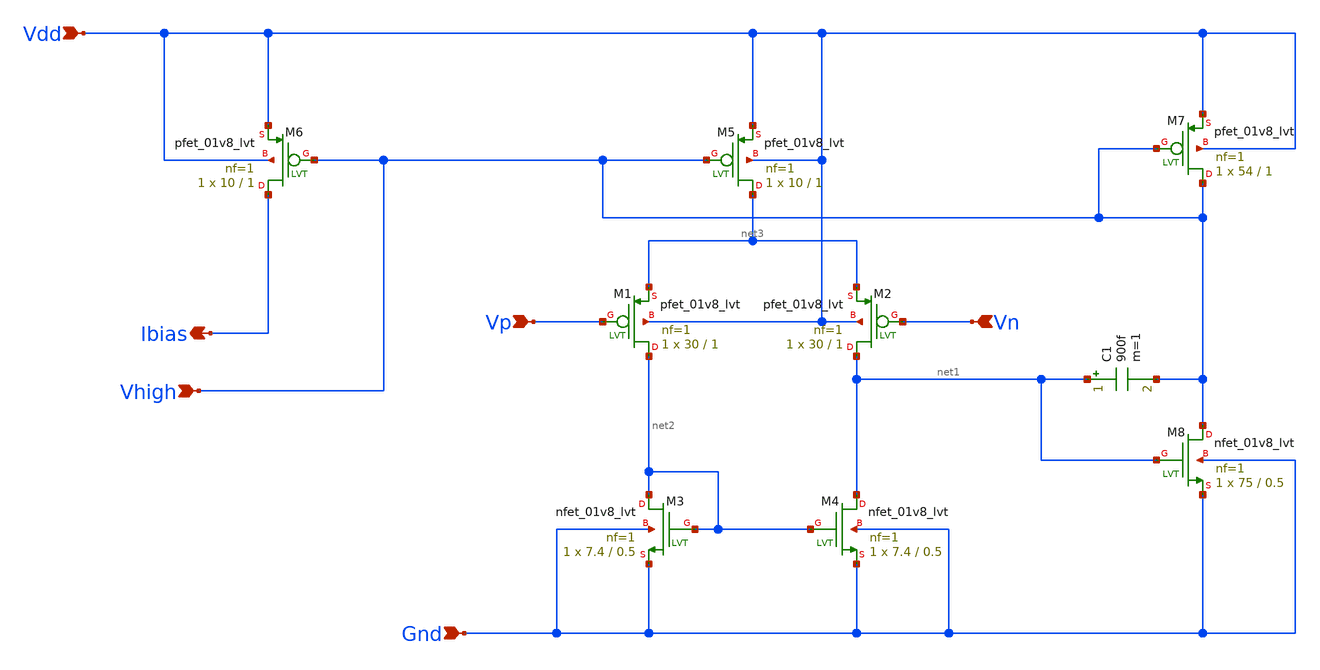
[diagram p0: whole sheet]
** sch_path: Bandgap/Schematics/BGR1.8v/Miller_OTA_PMOS.sch
**.subckt Miller_OTA_PMOS Vp Vn Ibias Vdd Gnd Vhigh
*.ipin Vp
*.ipin Vn
*.opin Ibias
*.ipin Vdd
*.ipin Gnd
*.ipin Vhigh
XM1 net2 Vp net3 Vdd sky130_fd_pr__pfet_01v8_lvt L=1 W=30 nf=1 ad='int((nf+1)/2) * W/nf * 0.29' as='int((nf+2)/2) * W/nf * 0.29'
+ pd='2*int((nf+1)/2) * (W/nf + 0.29)' ps='2*int((nf+2)/2) * (W/nf + 0.29)' nrd='0.29 / W' nrs='0.29 / W'
+ sa=0 sb=0 sd=0 mult=1 m=1
XM2 net1 Vn net3 Vdd sky130_fd_pr__pfet_01v8_lvt L=1 W=30 nf=1 ad='int((nf+1)/2) * W/nf * 0.29' as='int((nf+2)/2) * W/nf * 0.29'
+ pd='2*int((nf+1)/2) * (W/nf + 0.29)' ps='2*int((nf+2)/2) * (W/nf + 0.29)' nrd='0.29 / W' nrs='0.29 / W'
+ sa=0 sb=0 sd=0 mult=1 m=1
XM3 net2 net2 Gnd Gnd sky130_fd_pr__nfet_01v8_lvt L=0.5 W=7.4 nf=1 ad='int((nf+1)/2) * W/nf * 0.29' as='int((nf+2)/2) * W/nf * 0.29'
+ pd='2*int((nf+1)/2) * (W/nf + 0.29)' ps='2*int((nf+2)/2) * (W/nf + 0.29)' nrd='0.29 / W' nrs='0.29 / W'
+ sa=0 sb=0 sd=0 mult=1 m=1
XM4 net1 net2 Gnd Gnd sky130_fd_pr__nfet_01v8_lvt L=0.5 W=7.4 nf=1 ad='int((nf+1)/2) * W/nf * 0.29' as='int((nf+2)/2) * W/nf * 0.29'
+ pd='2*int((nf+1)/2) * (W/nf + 0.29)' ps='2*int((nf+2)/2) * (W/nf + 0.29)' nrd='0.29 / W' nrs='0.29 / W'
+ sa=0 sb=0 sd=0 mult=1 m=1
XM5 net3 Vhigh Vdd Vdd sky130_fd_pr__pfet_01v8_lvt L=1 W=10 nf=1 ad='int((nf+1)/2) * W/nf * 0.29' as='int((nf+2)/2) * W/nf * 0.29'
+ pd='2*int((nf+1)/2) * (W/nf + 0.29)' ps='2*int((nf+2)/2) * (W/nf + 0.29)' nrd='0.29 / W' nrs='0.29 / W'
+ sa=0 sb=0 sd=0 mult=1 m=1
XM6 Ibias Vhigh Vdd Vdd sky130_fd_pr__pfet_01v8_lvt L=1 W=10 nf=1 ad='int((nf+1)/2) * W/nf * 0.29' as='int((nf+2)/2) * W/nf * 0.29'
+ pd='2*int((nf+1)/2) * (W/nf + 0.29)' ps='2*int((nf+2)/2) * (W/nf + 0.29)' nrd='0.29 / W' nrs='0.29 / W'
+ sa=0 sb=0 sd=0 mult=1 m=1
XM7 Vhigh Vhigh Vdd Vdd sky130_fd_pr__pfet_01v8_lvt L=1 W=54 nf=1 ad='int((nf+1)/2) * W/nf * 0.29' as='int((nf+2)/2) * W/nf * 0.29'
+ pd='2*int((nf+1)/2) * (W/nf + 0.29)' ps='2*int((nf+2)/2) * (W/nf + 0.29)' nrd='0.29 / W' nrs='0.29 / W'
+ sa=0 sb=0 sd=0 mult=1 m=1
XM8 Vhigh net1 Gnd Gnd sky130_fd_pr__nfet_01v8_lvt L=0.5 W=75 nf=1 ad='int((nf+1)/2) * W/nf * 0.29' as='int((nf+2)/2) * W/nf * 0.29'
+ pd='2*int((nf+1)/2) * (W/nf + 0.29)' ps='2*int((nf+2)/2) * (W/nf + 0.29)' nrd='0.29 / W' nrs='0.29 / W'
+ sa=0 sb=0 sd=0 mult=1 m=1
C1 net1 Vhigh 900f m=1
**.ends
.end
